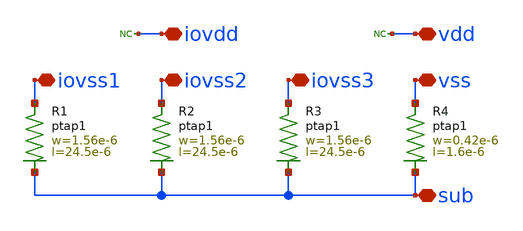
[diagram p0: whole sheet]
** sch_path: MSPHY6034-main/schematic/xschem/openpdk-libraries/ihp-sg13g2/sg13g2_io/xschem/sg13g2_Filler400.sch
**.subckt sg13g2_Filler400 iovss1 iovss2 iovss3 vss iovdd vdd sub
*.iopin iovss1
*.iopin iovss2
*.iopin iovss3
*.iopin vss
*.iopin iovdd
*.iopin vdd
*.iopin sub
XR3 iovss3 sub ptap1 R=10.85 w=1.56e-6 l=24.5e-6
XR4 vss sub ptap1 R=208 w=0.42e-6 l=1.6e-6
* noconn iovdd
* noconn vdd
XR1 iovss1 sub ptap1 R=10.85 w=1.56e-6 l=24.5e-6
XR2 iovss2 sub ptap1 R=10.85 w=1.56e-6 l=24.5e-6
**.ends
.end
